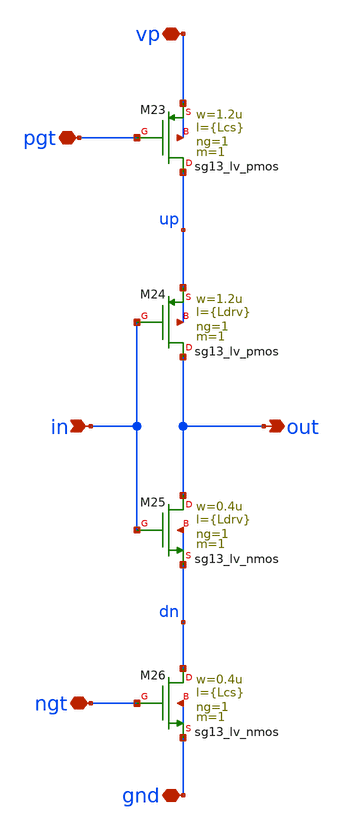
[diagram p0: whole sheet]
** sch_path: schematics/vco/vco_cell/vco_delay_cell_3BL.sch
**.subckt vco_delay_cell_3BL in out gnd vp pgt ngt
*.ipin in
*.opin out
*.iopin gnd
*.iopin vp
*.iopin pgt
*.iopin ngt
XM23 up pgt vp vp sg13_lv_pmos w=1.2u l={Lcs} ng=1 m=1 mm_ok=1
XM24 out in up up sg13_lv_pmos w=1.2u l={Ldrv} ng=1 m=1 mm_ok=1
XM25 out in dn dn sg13_lv_nmos w=0.4u l={Ldrv} ng=1 m=1 mm_ok=1
XM26 dn ngt gnd gnd sg13_lv_nmos w=0.4u l={Lcs} ng=1 m=1 mm_ok=1
**.ends
.end
